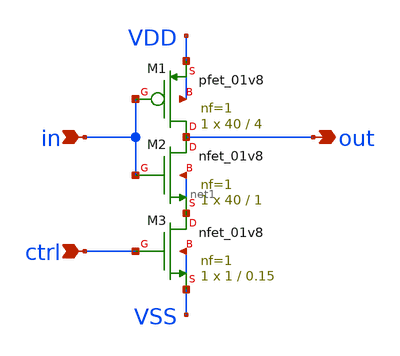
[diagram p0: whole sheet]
** sch_path: archive/tt_um_wulf_8bit_vco/xschem/lib/inv_strvd.sch
**.subckt inv_strvd in ctrl out
*.ipin in
*.ipin ctrl
*.opin out
XM2 out in net1 net1 sky130_fd_pr__nfet_01v8 L=1 W=40 nf=1 ad='int((1 + 1)/2) * 40 / 1 * 0.29' as='int((1 + 2)/2) * 40 / 1 * 0.29'
+ pd='2*int((1 + 1)/2) * (40 / 1 + 0.29)' ps='2*int((1 + 2)/2) * (40 / 1 + 0.29)' nrd='0.29 / 40 ' nrs='0.29 / 40 '
+ sa=0 sb=0 sd=0 mult=1 m=1
XM3 net1 ctrl VSS VSS sky130_fd_pr__nfet_01v8 L=0.15 W=1 nf=1 ad='int((1 + 1)/2) * 1 / 1 * 0.29' as='int((1 + 2)/2) * 1 / 1 * 0.29'
+ pd='2*int((1 + 1)/2) * (1 / 1 + 0.29)' ps='2*int((1 + 2)/2) * (1 / 1 + 0.29)' nrd='0.29 / 1 ' nrs='0.29 / 1 '
+ sa=0 sb=0 sd=0 mult=1 m=1
XM1 out in VDD VDD sky130_fd_pr__pfet_01v8 L=4 W=40 nf=1 ad='int((nf+1)/2) * W/nf * 0.29' as='int((nf+2)/2) * W/nf * 0.29'
+ pd='2*int((nf+1)/2) * (W/nf + 0.29)' ps='2*int((nf+2)/2) * (W/nf + 0.29)' nrd='0.29 / W' nrs='0.29 / W'
+ sa=0 sb=0 sd=0 mult=1 m=1
**.ends
.end
